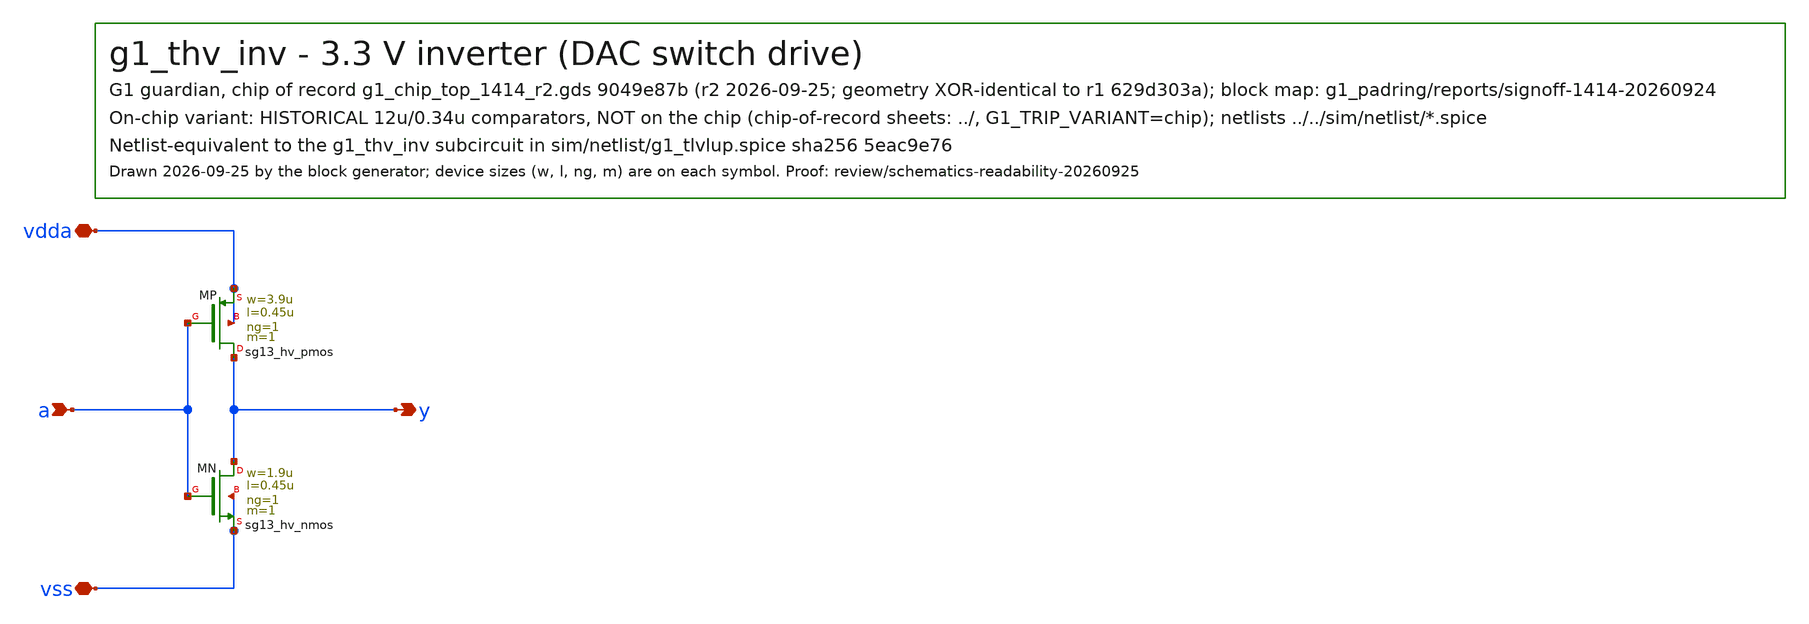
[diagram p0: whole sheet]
** sch_path: designs/g1-guardian/blocks/g1_trip/schematic/historical_12u034/g1_thv_inv.sch
**.subckt g1_thv_inv a y vdda vss
*.ipin a
*.opin y
*.iopin vdda
*.iopin vss
XMP y a vdda vdda sg13_hv_pmos w=3.9u l=0.45u ng=1 m=1 mm_ok=1
XMN y a vss vss sg13_hv_nmos w=1.9u l=0.45u ng=1 m=1 mm_ok=1
**.ends
.end
